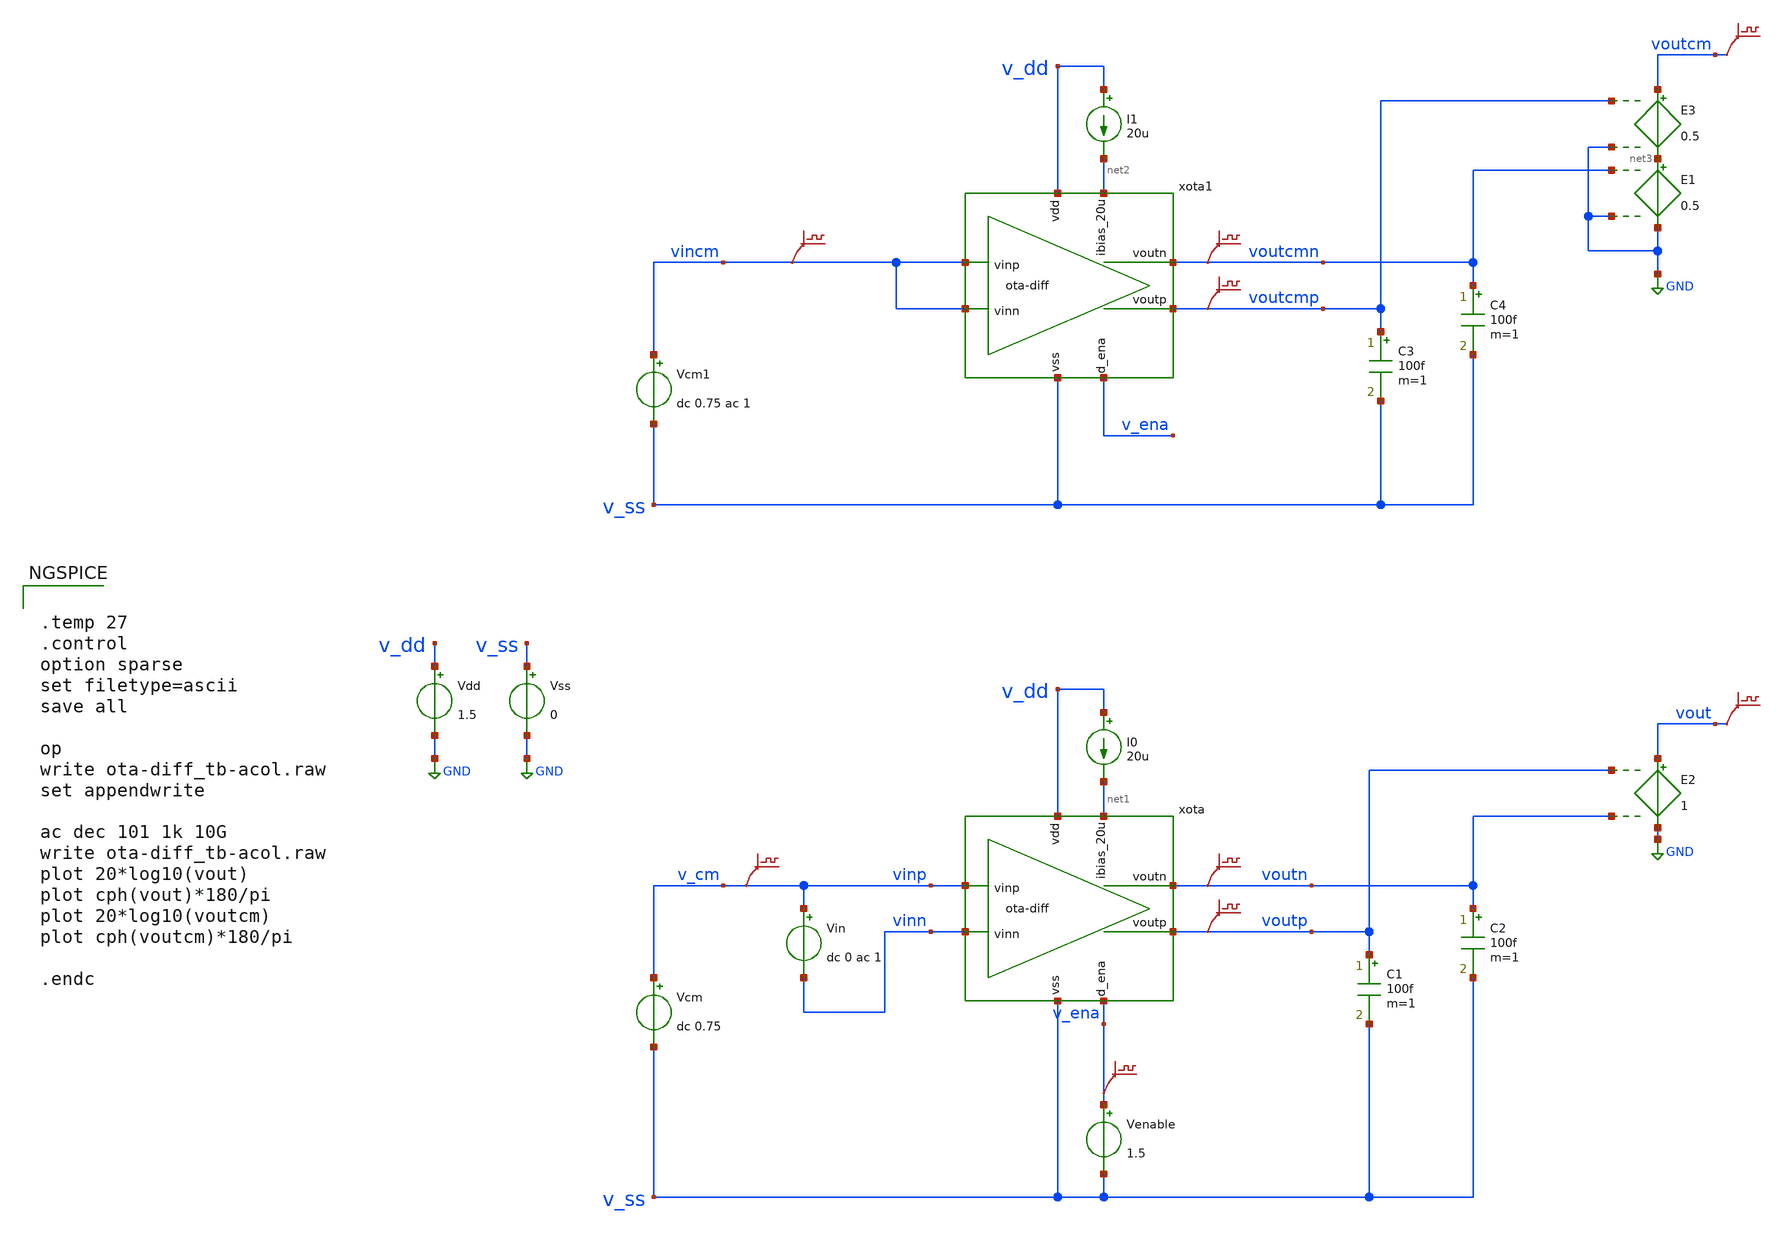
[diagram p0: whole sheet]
** sch_path: xschem/ota-diff_tb-acol.sch
* (c) 2024-2025 H. Pretl, Apache-2.0 license
* xschem/ota-diff.sch:
* (c) 2025 H. Pretl, Apache-2.0 license
**.subckt ota-diff_tb-acol
Vdd v_dd GND 1.5
xota v_dd v_cm vinn net1 v_ena v_ss voutn voutp ota-diff
Vss v_ss GND 0
C1 voutp v_ss 100f m=1
Vcm v_cm v_ss dc 0.75
I0 v_dd net1 20u
Venable v_ena v_ss 1.5
.save v(v_cm)
.save v(voutp)
.save v(v_ena)
Vin v_cm vinn dc 0 ac 1
C2 voutn v_ss 100f m=1
.save v(voutn)
xota1 v_dd vincm vincm net2 v_ena v_ss voutcmn voutcmp ota-diff
C3 voutcmp v_ss 100f m=1
Vcm1 vincm v_ss dc 0.75 ac 1
I1 v_dd net2 20u
.save v(vincm)
.save v(voutcmp)
C4 voutcmn v_ss 100f m=1
.save v(voutcmn)
E1 net3 GND voutcmn GND 0.5
.save v(voutcm)
E2 vout GND voutp voutn 1
.save v(vout)
E3 voutcm net3 voutcmp GND 0.5
**** begin user architecture code

.lib cornerMOSlv.lib mos_tt
.lib cornerRES.lib res_typ
.lib cornerCAP.lib cap_typ



.temp 27
.control
option sparse
set filetype=ascii
save all

op
write ota-diff_tb-acol.raw
set appendwrite

ac dec 101 1k 10G
write ota-diff_tb-acol.raw
plot 20*log10(vout)
plot cph(vout)*180/pi
plot 20*log10(voutcm)
plot cph(voutcm)*180/pi

.endc


**** end user architecture code
**.ends

* expanding   symbol:  ota-diff.sym # of pins=8
** sym_path: xschem/ota-diff.sym
** sch_path: xschem/ota-diff.sch
.subckt ota-diff vdd vinp vinn ibias_20u d_ena vss voutn voutp
*.ipin ibias_20u
*.iopin vdd
*.iopin vss
*.ipin vinp
*.ipin vinn
*.opin voutp
*.ipin d_ena
*.opin voutn
XM10 net6 gate_n net2 vss sg13_lv_nmos w=50u l=5u ng=10 m=1 mm_ok=1
XM1 tail vinp vintn vss sg13_lv_nmos w=10u l=0.5u ng=2 m=1 mm_ok=1
XM2 tail vinn vintp vss sg13_lv_nmos w=10u l=0.5u ng=2 m=1 mm_ok=1
XM3 vintn gate_p vdd vdd sg13_lv_pmos w=10u l=0.5u ng=2 m=1 mm_ok=1
XM9 net4 gate_n ibias_20u vss sg13_lv_nmos w=5u l=5u ng=1 m=1 mm_ok=1
XM16 vss ena_n gate_n vss sg13_lv_nmos w=5u l=0.13u ng=1 m=1 mm_ok=1
XM18 gate_p ena vdd vdd sg13_lv_pmos w=5u l=0.13u ng=1 m=1 mm_ok=1
XM14 vss ena_n ena vss sg13_lv_nmos w=5u l=0.13u ng=1 m=1 mm_ok=1
XM15 ena ena_n vdd vdd sg13_lv_pmos w=5u l=0.13u ng=1 m=1 mm_ok=1
XM17 gate_n ena ibias_20u vss sg13_lv_nmos w=5u l=0.13u ng=1 m=1 mm_ok=1
XM12 vss d_ena ena_n vss sg13_lv_nmos w=5u l=0.13u ng=1 m=1 mm_ok=1
XM13 ena_n d_ena vdd vdd sg13_lv_pmos w=5u l=0.13u ng=1 m=1 mm_ok=1
XM7 vss net1 voutp vss sg13_lv_nmos w=20u l=5u ng=4 m=1 mm_ok=1
XR1 gate_p vintn sub! rhigh w=0.5e-6 l=35e-6 m=1 b=0 mm_ok=1
XR3 net1 voutp sub! rhigh w=0.5e-6 l=60e-6 m=1 b=0 mm_ok=1
XM11_1 net5 gate_n net3 vss sg13_lv_nmos w=1u l=5u ng=1 m=1 mm_ok=1
XM5 vintp gate_p vdd vdd sg13_lv_pmos w=10u l=0.5u ng=2 m=1 mm_ok=1
XM4 net7 vintn vdd vdd sg13_lv_pmos w=10u l=0.5u ng=2 m=1 mm_ok=1
XM6 net8 vintp vdd vdd sg13_lv_pmos w=10u l=0.5u ng=2 m=1 mm_ok=1
XR2 gate_p vintp sub! rhigh w=0.5e-6 l=35e-6 m=1 b=0 mm_ok=1
XM8 vss net1 voutn vss sg13_lv_nmos w=20u l=5u ng=4 m=1 mm_ok=1
XR4 net1 voutn sub! rhigh w=0.5e-6 l=60e-6 m=1 b=0 mm_ok=1
Vmeas tail net2 0
.save i(vmeas)
Vmeas1 net7 voutp 0
.save i(vmeas1)
Vmeas2 net8 voutn 0
.save i(vmeas2)
Vmeas3 net1 net3 0
.save i(vmeas3)
XR51 net4 vss sub! rhigh w=0.5e-6 l=5e-6 m=1 b=0 mm_ok=1
XR52 net4 vss sub! rhigh w=0.5e-6 l=5e-6 m=1 b=0 mm_ok=1
XR53 net4 vss sub! rhigh w=0.5e-6 l=5e-6 m=1 b=0 mm_ok=1
XR7 net5 vss sub! rhigh w=0.5e-6 l=20e-6 m=1 b=0 mm_ok=1
XR61 net6 vss sub! rhigh w=0.5e-6 l=5e-6 m=1 b=0 mm_ok=1
XR62 net6 vss sub! rhigh w=0.5e-6 l=5e-6 m=1 b=0 mm_ok=1
XR63 net6 vss sub! rhigh w=0.5e-6 l=5e-6 m=1 b=0 mm_ok=1
XR64 net6 vss sub! rhigh w=0.5e-6 l=5e-6 m=1 b=0 mm_ok=1
XR65 net6 vss sub! rhigh w=0.5e-6 l=5e-6 m=1 b=0 mm_ok=1
XR66 net6 vss sub! rhigh w=0.5e-6 l=5e-6 m=1 b=0 mm_ok=1
XR67 net6 vss sub! rhigh w=0.5e-6 l=5e-6 m=1 b=0 mm_ok=1
XR68 net6 vss sub! rhigh w=0.5e-6 l=5e-6 m=1 b=0 mm_ok=1
XR69 net6 vss sub! rhigh w=0.5e-6 l=5e-6 m=1 b=0 mm_ok=1
XR610 net6 vss sub! rhigh w=0.5e-6 l=5e-6 m=1 b=0 mm_ok=1
XR611 net6 vss sub! rhigh w=0.5e-6 l=5e-6 m=1 b=0 mm_ok=1
XR612 net6 vss sub! rhigh w=0.5e-6 l=5e-6 m=1 b=0 mm_ok=1
XR613 net6 vss sub! rhigh w=0.5e-6 l=5e-6 m=1 b=0 mm_ok=1
XR614 net6 vss sub! rhigh w=0.5e-6 l=5e-6 m=1 b=0 mm_ok=1
XR615 net6 vss sub! rhigh w=0.5e-6 l=5e-6 m=1 b=0 mm_ok=1
XR616 net6 vss sub! rhigh w=0.5e-6 l=5e-6 m=1 b=0 mm_ok=1
XR617 net6 vss sub! rhigh w=0.5e-6 l=5e-6 m=1 b=0 mm_ok=1
XR618 net6 vss sub! rhigh w=0.5e-6 l=5e-6 m=1 b=0 mm_ok=1
XR619 net6 vss sub! rhigh w=0.5e-6 l=5e-6 m=1 b=0 mm_ok=1
XR620 net6 vss sub! rhigh w=0.5e-6 l=5e-6 m=1 b=0 mm_ok=1
XR621 net6 vss sub! rhigh w=0.5e-6 l=5e-6 m=1 b=0 mm_ok=1
XR622 net6 vss sub! rhigh w=0.5e-6 l=5e-6 m=1 b=0 mm_ok=1
XR623 net6 vss sub! rhigh w=0.5e-6 l=5e-6 m=1 b=0 mm_ok=1
XR624 net6 vss sub! rhigh w=0.5e-6 l=5e-6 m=1 b=0 mm_ok=1
XR625 net6 vss sub! rhigh w=0.5e-6 l=5e-6 m=1 b=0 mm_ok=1
XR626 net6 vss sub! rhigh w=0.5e-6 l=5e-6 m=1 b=0 mm_ok=1
XR627 net6 vss sub! rhigh w=0.5e-6 l=5e-6 m=1 b=0 mm_ok=1
XR628 net6 vss sub! rhigh w=0.5e-6 l=5e-6 m=1 b=0 mm_ok=1
XR629 net6 vss sub! rhigh w=0.5e-6 l=5e-6 m=1 b=0 mm_ok=1
XR630 net6 vss sub! rhigh w=0.5e-6 l=5e-6 m=1 b=0 mm_ok=1
XCM3 gate_p net10 cap_cmim w=80e-6 l=20e-6 m=1 mm_ok=1
XCM4 gate_p net9 cap_cmim w=80e-6 l=20e-6 m=1 mm_ok=1
XR81 net10 vintn sub! rppd w=0.5e-6 l=5e-6 m=1 b=0 mm_ok=1
XR82 net10 vintn sub! rppd w=0.5e-6 l=5e-6 m=1 b=0 mm_ok=1
XR83 net10 vintn sub! rppd w=0.5e-6 l=5e-6 m=1 b=0 mm_ok=1
XR84 net10 vintn sub! rppd w=0.5e-6 l=5e-6 m=1 b=0 mm_ok=1
XR11 net9 vintp sub! rppd w=0.5e-6 l=5e-6 m=1 b=0 mm_ok=1
XR12 net9 vintp sub! rppd w=0.5e-6 l=5e-6 m=1 b=0 mm_ok=1
XR13 net9 vintp sub! rppd w=0.5e-6 l=5e-6 m=1 b=0 mm_ok=1
XR14 net9 vintp sub! rppd w=0.5e-6 l=5e-6 m=1 b=0 mm_ok=1
.ends

.GLOBAL GND
.end
